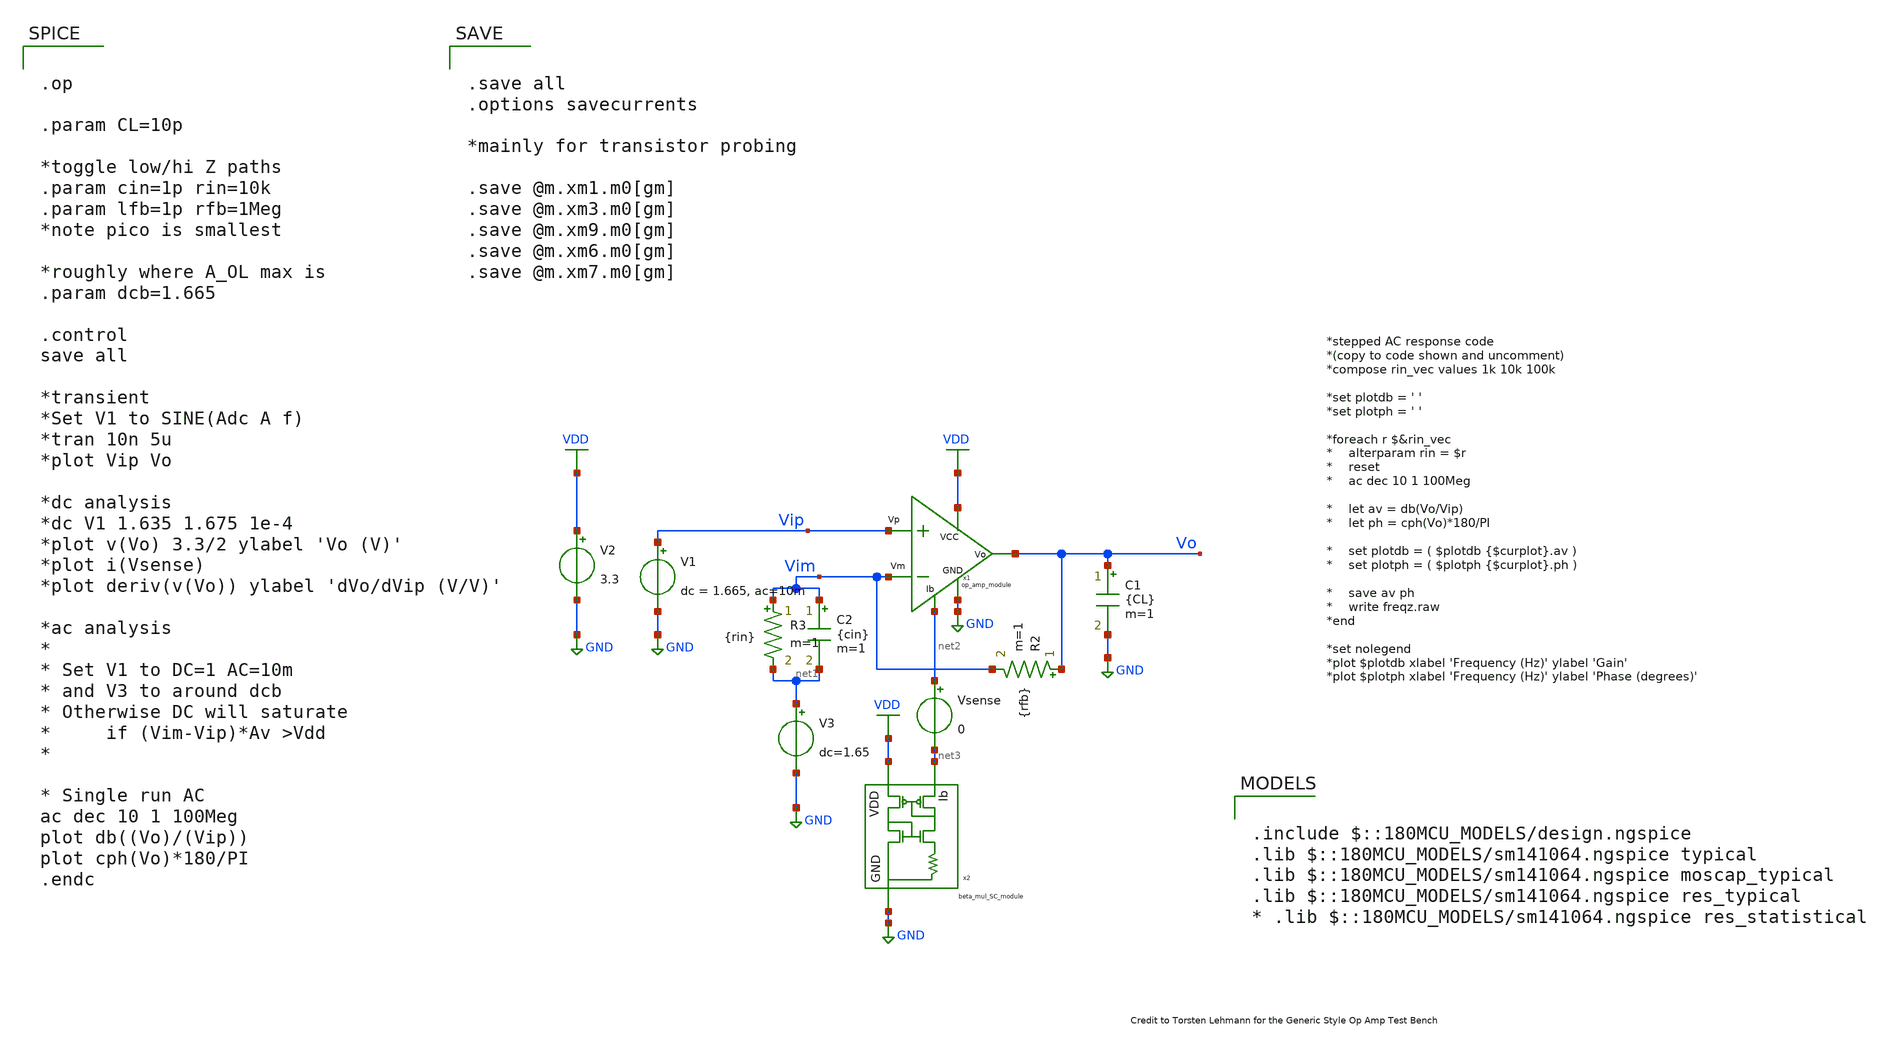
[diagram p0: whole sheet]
** sch_path: op_beta_tb.sch
**.subckt op_beta_tb
x1 VDD Vo Vip Vim net2 GND op_amp_module
V1 Vip GND dc = 1.665, ac=10m
V2 VDD GND 3.3
C1 Vo GND {CL} m=1
R2 Vo Vim {rfb} m=1
R3 Vim net1 {rin} m=1
V3 net1 GND dc=1.65
C2 Vim net1 {cin} m=1
x2 VDD net3 GND beta_mul_SC_module
Vsense net2 net3 0
**** begin user architecture code


.op

.param CL=10p

*toggle low/hi Z paths
.param cin=1p rin=10k
.param lfb=1p rfb=1Meg
*note pico is smallest

*roughly where A_OL max is
.param dcb=1.665

.control
save all

*transient
*Set V1 to SINE(Adc A f)
*tran 10n 5u
*plot Vip Vo

*dc analysis
*dc V1 1.635 1.675 1e-4
*plot v(Vo) 3.3/2 ylabel 'Vo (V)'
*plot i(Vsense)
*plot deriv(v(Vo)) ylabel 'dVo/dVip (V/V)'

*ac analysis
*
* Set V1 to DC=1 AC=10m
* and V3 to around dcb
* Otherwise DC will saturate
* 	if (Vim-Vip)*Av >Vdd
*

* Single run AC
ac dec 10 1 100Meg
plot db((Vo)/(Vip))
plot cph(Vo)*180/PI
.endc




.save all
.options savecurrents

*mainly for transistor probing

.save @m.xm1.m0[gm]
.save @m.xm3.m0[gm]
.save @m.xm9.m0[gm]
.save @m.xm6.m0[gm]
.save @m.xm7.m0[gm]




.include $::180MCU_MODELS/design.ngspice
.lib $::180MCU_MODELS/sm141064.ngspice typical
.lib $::180MCU_MODELS/sm141064.ngspice moscap_typical
.lib $::180MCU_MODELS/sm141064.ngspice res_typical
* .lib $::180MCU_MODELS/sm141064.ngspice res_statistical

**** end user architecture code
**.ends

* expanding   symbol:  op_amp_module.sym # of pins=6
** sym_path: op_amp_module.sym
** sch_path: op_amp_module.sch
.subckt op_amp_module Vcc Vo Vp Vm Ib GND
*.ipin Vm
*.ipin Vp
*.ipin Vcc
*.ipin GND
*.opin Ib
*.opin Vo
XM4 net3 net3 net4 GND nfet_03v3 L=0.3u W=6.25u nf=1 ad='int((nf+1)/2) * W/nf * 0.18u' as='int((nf+2)/2) * W/nf * 0.18u'
+ pd='2*int((nf+1)/2) * (W/nf + 0.18u)' ps='2*int((nf+2)/2) * (W/nf + 0.18u)' nrd='0.18u / W' nrs='0.18u / W'
+ sa=0 sb=0 sd=0 m=1 par=1
XM2 net3 Vm net1 Vcc pfet_03v3 L=0.3u W=5.5u nf=1 ad='int((nf+1)/2) * W/nf * 0.18u' as='int((nf+2)/2) * W/nf * 0.18u'
+ pd='2*int((nf+1)/2) * (W/nf + 0.18u)' ps='2*int((nf+2)/2) * (W/nf + 0.18u)' nrd='0.18u / W' nrs='0.18u / W'
+ sa=0 sb=0 sd=0 m=1 par=1
XM3 net2 net3 net5 GND nfet_03v3 L=0.3u W=6.25u nf=1 ad='int((nf+1)/2) * W/nf * 0.18u' as='int((nf+2)/2) * W/nf * 0.18u'
+ pd='2*int((nf+1)/2) * (W/nf + 0.18u)' ps='2*int((nf+2)/2) * (W/nf + 0.18u)' nrd='0.18u / W' nrs='0.18u / W'
+ sa=0 sb=0 sd=0 m=1 par=1
XM1 net2 Vp net1 Vcc pfet_03v3 L=0.3u W=5.5u nf=1 ad='int((nf+1)/2) * W/nf * 0.18u' as='int((nf+2)/2) * W/nf * 0.18u'
+ pd='2*int((nf+1)/2) * (W/nf + 0.18u)' ps='2*int((nf+2)/2) * (W/nf + 0.18u)' nrd='0.18u / W' nrs='0.18u / W'
+ sa=0 sb=0 sd=0 m=1 par=1
XM5 net1 Ib Vcc Vcc pfet_03v3 L=0.3u W=24u nf=1 ad='int((nf+1)/2) * W/nf * 0.18u' as='int((nf+2)/2) * W/nf * 0.18u'
+ pd='2*int((nf+1)/2) * (W/nf + 0.18u)' ps='2*int((nf+2)/2) * (W/nf + 0.18u)' nrd='0.18u / W' nrs='0.18u / W'
+ sa=0 sb=0 sd=0 m=1 par=1
XM6 Vo Ib Vcc Vcc pfet_03v3 L=0.3u W=24u nf=1 ad='int((nf+1)/2) * W/nf * 0.18u' as='int((nf+2)/2) * W/nf * 0.18u'
+ pd='2*int((nf+1)/2) * (W/nf + 0.18u)' ps='2*int((nf+2)/2) * (W/nf + 0.18u)' nrd='0.18u / W' nrs='0.18u / W'
+ sa=0 sb=0 sd=0 m=1 par=1
XM8 Ib Ib Vcc Vcc pfet_03v3 L=0.3u W=24u nf=1 ad='int((nf+1)/2) * W/nf * 0.18u' as='int((nf+2)/2) * W/nf * 0.18u'
+ pd='2*int((nf+1)/2) * (W/nf + 0.18u)' ps='2*int((nf+2)/2) * (W/nf + 0.18u)' nrd='0.18u / W' nrs='0.18u / W'
+ sa=0 sb=0 sd=0 m=1 par=1
XM7 Vo net2 GND GND nfet_03v3 L=0.3u W=6.25u nf=1 ad='int((nf+1)/2) * W/nf * 0.18u' as='int((nf+2)/2) * W/nf * 0.18u'
+ pd='2*int((nf+1)/2) * (W/nf + 0.18u)' ps='2*int((nf+2)/2) * (W/nf + 0.18u)' nrd='0.18u / W' nrs='0.18u / W'
+ sa=0 sb=0 sd=0 m=1 par=1
XM10 net4 net4 GND GND nfet_03v3 L=0.3u W=6.25u nf=1 ad='int((nf+1)/2) * W/nf * 0.18u' as='int((nf+2)/2) * W/nf * 0.18u'
+ pd='2*int((nf+1)/2) * (W/nf + 0.18u)' ps='2*int((nf+2)/2) * (W/nf + 0.18u)' nrd='0.18u / W' nrs='0.18u / W'
+ sa=0 sb=0 sd=0 m=1 par=1
XM9 net5 net4 GND GND nfet_03v3 L=0.3u W=6.25u nf=1 ad='int((nf+1)/2) * W/nf * 0.18u' as='int((nf+2)/2) * W/nf * 0.18u'
+ pd='2*int((nf+1)/2) * (W/nf + 0.18u)' ps='2*int((nf+2)/2) * (W/nf + 0.18u)' nrd='0.18u / W' nrs='0.18u / W'
+ sa=0 sb=0 sd=0 m=1 par=1
XC2 net5 Vo cap_pmos_03v3 c_width=18u c_length=18u m=1
.ends


* expanding   symbol:  beta_mul_SC_module.sym # of pins=3
** sym_path: beta_mul_SC_module.sym
** sch_path: beta_mul_SC_module.sch
.subckt beta_mul_SC_module VDD Ib GND
*.ipin VDD
*.ipin GND
*.ipin Ib
XM1 net1 Nbias GND GND nfet_03v3 L=0.6u W=15u nf=1 ad='int((nf+1)/2) * W/nf * 0.18u' as='int((nf+2)/2) * W/nf * 0.18u'
+ pd='2*int((nf+1)/2) * (W/nf + 0.18u)' ps='2*int((nf+2)/2) * (W/nf + 0.18u)' nrd='0.18u / W' nrs='0.18u / W'
+ sa=0 sb=0 sd=0 m=1 par=1
XM2 net1 net1 VDD VDD pfet_03v3 L=6u W=3u nf=1 ad='int((nf+1)/2) * W/nf * 0.18u' as='int((nf+2)/2) * W/nf * 0.18u'
+ pd='2*int((nf+1)/2) * (W/nf + 0.18u)' ps='2*int((nf+2)/2) * (W/nf + 0.18u)' nrd='0.18u / W' nrs='0.18u / W'
+ sa=0 sb=0 sd=0 m=1 par=1
XM3 Pbias net1 Nbias GND nfet_03v3 L=0.3u W=3u nf=1 ad='int((nf+1)/2) * W/nf * 0.18u' as='int((nf+2)/2) * W/nf * 0.18u'
+ pd='2*int((nf+1)/2) * (W/nf + 0.18u)' ps='2*int((nf+2)/2) * (W/nf + 0.18u)' nrd='0.18u / W' nrs='0.18u / W'
+ sa=0 sb=0 sd=0 m=1 par=1
XM4 Nbias Nbias GND GND nfet_03v3 L=0.6u W=15u nf=1 ad='int((nf+1)/2) * W/nf * 0.18u' as='int((nf+2)/2) * W/nf * 0.18u'
+ pd='2*int((nf+1)/2) * (W/nf + 0.18u)' ps='2*int((nf+2)/2) * (W/nf + 0.18u)' nrd='0.18u / W' nrs='0.18u / W'
+ sa=0 sb=0 sd=0 m=1 par=1
XM5 net3 net2 GND GND nfet_03v3 L=0.6u W=15u nf=1 ad='int((nf+1)/2) * W/nf * 0.18u' as='int((nf+2)/2) * W/nf * 0.18u'
+ pd='2*int((nf+1)/2) * (W/nf + 0.18u)' ps='2*int((nf+2)/2) * (W/nf + 0.18u)' nrd='0.18u / W' nrs='0.18u / W'
+ sa=0 sb=0 sd=0 m=1 par=1
XM6 Pbias Nbias GND GND nfet_03v3 L=0.6u W=15u nf=1 ad='int((nf+1)/2) * W/nf * 0.18u' as='int((nf+2)/2) * W/nf * 0.18u'
+ pd='2*int((nf+1)/2) * (W/nf + 0.18u)' ps='2*int((nf+2)/2) * (W/nf + 0.18u)' nrd='0.18u / W' nrs='0.18u / W'
+ sa=0 sb=0 sd=0 m=1 par=1
XM7 net2 net2 net4 GND nfet_03v3 L=0.6u W=60u nf=1 ad='int((nf+1)/2) * W/nf * 0.18u' as='int((nf+2)/2) * W/nf * 0.18u'
+ pd='2*int((nf+1)/2) * (W/nf + 0.18u)' ps='2*int((nf+2)/2) * (W/nf + 0.18u)' nrd='0.18u / W' nrs='0.18u / W'
+ sa=0 sb=0 sd=0 m=1 par=1
XM9 Nbias Pbias VDD VDD pfet_03v3 L=0.6u W=30u nf=1 ad='int((nf+1)/2) * W/nf * 0.18u' as='int((nf+2)/2) * W/nf * 0.18u'
+ pd='2*int((nf+1)/2) * (W/nf + 0.18u)' ps='2*int((nf+2)/2) * (W/nf + 0.18u)' nrd='0.18u / W' nrs='0.18u / W'
+ sa=0 sb=0 sd=0 m=1 par=1
XM10 net3 net3 VDD VDD pfet_03v3 L=0.6u W=30u nf=1 ad='int((nf+1)/2) * W/nf * 0.18u' as='int((nf+2)/2) * W/nf * 0.18u'
+ pd='2*int((nf+1)/2) * (W/nf + 0.18u)' ps='2*int((nf+2)/2) * (W/nf + 0.18u)' nrd='0.18u / W' nrs='0.18u / W'
+ sa=0 sb=0 sd=0 m=1 par=1
XM11 Pbias net3 VDD VDD pfet_03v3 L=0.6u W=30u nf=1 ad='int((nf+1)/2) * W/nf * 0.18u' as='int((nf+2)/2) * W/nf * 0.18u'
+ pd='2*int((nf+1)/2) * (W/nf + 0.18u)' ps='2*int((nf+2)/2) * (W/nf + 0.18u)' nrd='0.18u / W' nrs='0.18u / W'
+ sa=0 sb=0 sd=0 m=1 par=1
XM12 net2 Pbias VDD VDD pfet_03v3 L=0.6u W=30u nf=1 ad='int((nf+1)/2) * W/nf * 0.18u' as='int((nf+2)/2) * W/nf * 0.18u'
+ pd='2*int((nf+1)/2) * (W/nf + 0.18u)' ps='2*int((nf+2)/2) * (W/nf + 0.18u)' nrd='0.18u / W' nrs='0.18u / W'
+ sa=0 sb=0 sd=0 m=1 par=1
XM8 Ib Nbias GND GND nfet_03v3 L=0.6u W=7.5u nf=1 ad='int((nf+1)/2) * W/nf * 0.18u' as='int((nf+2)/2) * W/nf * 0.18u'
+ pd='2*int((nf+1)/2) * (W/nf + 0.18u)' ps='2*int((nf+2)/2) * (W/nf + 0.18u)' nrd='0.18u / W' nrs='0.18u / W'
+ sa=0 sb=0 sd=0 m=1 par=1
XC1 Nbias GND cap_nmos_03v3 c_width=20u c_length=20u m=1
XC2 Pbias VDD cap_pmos_03v3 c_width=20u c_length=20u m=1
XR1 GND net4 GND npolyf_u r_width=5u r_length=52.5u m=1
.ends

.GLOBAL GND
.GLOBAL VDD
.end
